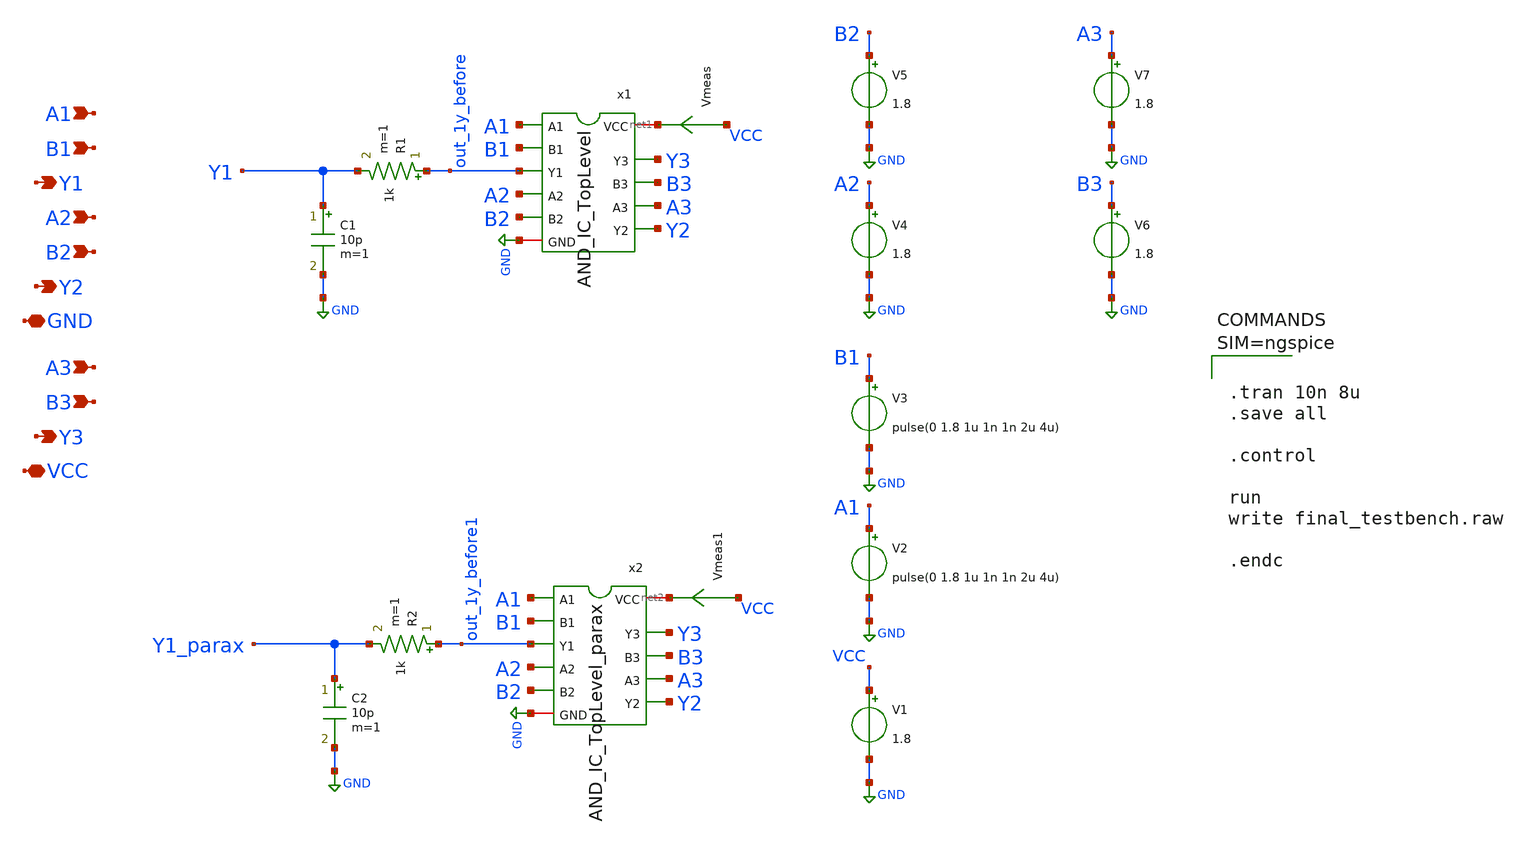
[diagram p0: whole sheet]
** sch_path: xschem/ic_7408_testbench.sch
**.subckt ic_7408_testbench A1 GND Y1 B1 A2 B2 A3 Y2 Y3 VCC B3
*.ipin A1
*.iopin GND
*.opin Y1
*.ipin B1
*.ipin A2
*.ipin B2
*.ipin A3
*.opin Y2
*.opin Y3
*.iopin VCC
*.ipin B3
V1 VCC GND 1.8
V2 A1 GND pulse(0 1.8 1u 1n 1n 2u 4u)
V3 B1 GND pulse(0 1.8 1u 1n 1n 2u 4u)
R1 out_1y_before Y1 1k m=1
C1 Y1 GND 10p m=1
Vmeas VCC net1 0
.save i(vmeas)
V4 A2 GND 1.8
V5 B2 GND 1.8
V6 B3 GND 1.8
V7 A3 GND 1.8
x1 A1 B1 out_1y_before A2 B2 Y2 GND A3 B3 Y3 net1 AND_IC_TopLevel
R2 out_1y_before1 Y1_parax 1k m=1
C2 Y1_parax GND 10p m=1
Vmeas1 VCC net2 0
.save i(vmeas1)
x2 A1 B1 out_1y_before1 A2 B2 Y2 GND A3 B3 Y3 net2 AND_IC_TopLevel_parax
**** begin user architecture code

** opencircuitdesign pdks install
.lib $::SKYWATER_MODELS/sky130.lib.spice tt





.tran 10n 8u
.save all

.control

run
write final_testbench.raw

.endc



**** end user architecture code
**.ends

* expanding   symbol:  AND_IC_TopLevel.sym # of pins=11
** sym_path: xschem/AND_IC_TopLevel.sym
** sch_path: xschem/AND_IC_TopLevel.sch
.subckt AND_IC_TopLevel A1 B1 Y1 A2 B2 Y2 GND A3 B3 Y3 VCC
*.ipin A1
*.iopin GND
*.opin Y1
*.ipin B1
*.ipin A2
*.ipin B2
*.ipin A3
*.opin Y2
*.opin Y3
*.iopin VCC
*.ipin B3
x1 A1 B1 Y1 VCC GND ic_7804_AND
x2 A2 B2 Y2 VCC GND ic_7804_AND
x3 A3 B3 Y3 VCC GND ic_7804_AND
.ends


* expanding   symbol:  AND_IC_TopLevel_parax.sym # of pins=11
** sym_path: xschem/AND_IC_TopLevel.sym
.include [file normalize ../mag/AND_IC_TopLevel.sim.spice]

* expanding   symbol:  ic_7804_AND.sym # of pins=5
** sym_path: xschem/ic_7804_AND.sym
** sch_path: xschem/ic_7804_AND.sch
.subckt ic_7804_AND A B Y VCC GND
*.ipin A
*.opin Y
*.ipin B
*.iopin VCC
*.iopin GND
XM2 net1 A VCC VCC sky130_fd_pr__pfet_01v8 L=0.15 W=2 nf=1 ad='int((nf+1)/2) * W/nf * 0.29' as='int((nf+2)/2) * W/nf * 0.29'
+ pd='2*int((nf+1)/2) * (W/nf + 0.29)' ps='2*int((nf+2)/2) * (W/nf + 0.29)' nrd='0.29 / W' nrs='0.29 / W'
+ sa=0 sb=0 sd=0 mult=1 m=1
XM3 net1 B VCC VCC sky130_fd_pr__pfet_01v8 L=0.15 W=2 nf=1 ad='int((nf+1)/2) * W/nf * 0.29' as='int((nf+2)/2) * W/nf * 0.29'
+ pd='2*int((nf+1)/2) * (W/nf + 0.29)' ps='2*int((nf+2)/2) * (W/nf + 0.29)' nrd='0.29 / W' nrs='0.29 / W'
+ sa=0 sb=0 sd=0 mult=1 m=1
XM5 Y net1 VCC VCC sky130_fd_pr__pfet_01v8 L=0.15 W=2 nf=1 ad='int((nf+1)/2) * W/nf * 0.29' as='int((nf+2)/2) * W/nf * 0.29'
+ pd='2*int((nf+1)/2) * (W/nf + 0.29)' ps='2*int((nf+2)/2) * (W/nf + 0.29)' nrd='0.29 / W' nrs='0.29 / W'
+ sa=0 sb=0 sd=0 mult=1 m=1
XM1 net1 A net2 GND sky130_fd_pr__nfet_01v8 L=0.15 W=1 nf=1 ad='int((nf+1)/2) * W/nf * 0.29' as='int((nf+2)/2) * W/nf * 0.29'
+ pd='2*int((nf+1)/2) * (W/nf + 0.29)' ps='2*int((nf+2)/2) * (W/nf + 0.29)' nrd='0.29 / W' nrs='0.29 / W'
+ sa=0 sb=0 sd=0 mult=1 m=1
XM4 net2 B GND GND sky130_fd_pr__nfet_01v8 L=0.15 W=1 nf=1 ad='int((nf+1)/2) * W/nf * 0.29' as='int((nf+2)/2) * W/nf * 0.29'
+ pd='2*int((nf+1)/2) * (W/nf + 0.29)' ps='2*int((nf+2)/2) * (W/nf + 0.29)' nrd='0.29 / W' nrs='0.29 / W'
+ sa=0 sb=0 sd=0 mult=1 m=1
XM6 Y net1 GND GND sky130_fd_pr__nfet_01v8 L=0.15 W=1 nf=1 ad='int((nf+1)/2) * W/nf * 0.29' as='int((nf+2)/2) * W/nf * 0.29'
+ pd='2*int((nf+1)/2) * (W/nf + 0.29)' ps='2*int((nf+2)/2) * (W/nf + 0.29)' nrd='0.29 / W' nrs='0.29 / W'
+ sa=0 sb=0 sd=0 mult=1 m=1
.ends

.GLOBAL GND
.end
